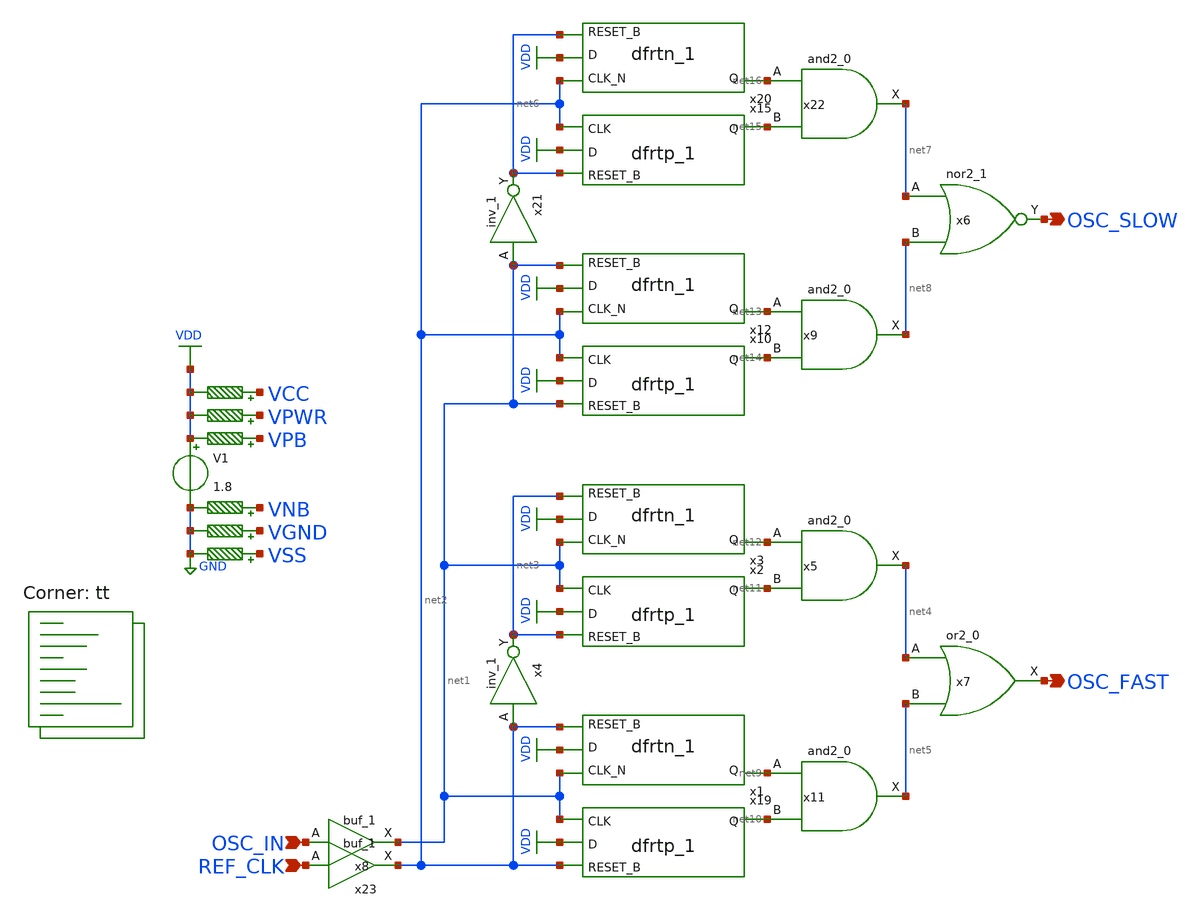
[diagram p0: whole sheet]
** sch_path: freq_det.sch
**.subckt freq_det OSC_IN REF_CLK OSC_FAST OSC_SLOW
*.ipin OSC_IN
*.ipin REF_CLK
*.opin OSC_FAST
*.opin OSC_SLOW
x8 OSC_IN VGND VNB VPB VPWR net1 sky130_fd_sc_hd__buf_1
x7 net4 net5 VGND VNB VPB VPWR OSC_FAST sky130_fd_sc_hd__or2_0
x11 net9 net10 VGND VNB VPB VPWR net5 sky130_fd_sc_hd__and2_0
x19 net1 VDD net2 VGND VNB VPB VPWR net10 sky130_fd_sc_hd__dfrtp_1
x1 net1 VDD net2 VGND VNB VPB VPWR net9 sky130_fd_sc_hd__dfrtn_1
x2 net1 VDD net3 VGND VNB VPB VPWR net11 sky130_fd_sc_hd__dfrtp_1
x3 net1 VDD net3 VGND VNB VPB VPWR net12 sky130_fd_sc_hd__dfrtn_1
x4 net2 VGND VNB VPB VPWR net3 sky130_fd_sc_hd__inv_1
x5 net12 net11 VGND VNB VPB VPWR net4 sky130_fd_sc_hd__and2_0
x9 net13 net14 VGND VNB VPB VPWR net8 sky130_fd_sc_hd__and2_0
x10 net2 VDD net1 VGND VNB VPB VPWR net14 sky130_fd_sc_hd__dfrtp_1
x12 net2 VDD net1 VGND VNB VPB VPWR net13 sky130_fd_sc_hd__dfrtn_1
x15 net2 VDD net6 VGND VNB VPB VPWR net15 sky130_fd_sc_hd__dfrtp_1
x20 net2 VDD net6 VGND VNB VPB VPWR net16 sky130_fd_sc_hd__dfrtn_1
x21 net1 VGND VNB VPB VPWR net6 sky130_fd_sc_hd__inv_1
x22 net16 net15 VGND VNB VPB VPWR net7 sky130_fd_sc_hd__and2_0
x6 net7 net8 VGND VNB VPB VPWR OSC_SLOW sky130_fd_sc_hd__nor2_1
x23 REF_CLK VGND VNB VPB VPWR net2 sky130_fd_sc_hd__buf_1
V1 VDD GND 1.8
R1 VPB VDD 0.01 m=1
R2 VPWR VDD 0.01 m=1
R3 VCC VDD 0.01 m=1
R4 VNB GND 0.01 m=1
R5 VGND GND 0.01 m=1
R6 VSS GND 0.01 m=1
**** begin user architecture code
.lib $::SKYWATER_MODELS/sky130.lib.spice tt


.include /usr/local/share/pdk/sky130A/libs.ref/sky130_fd_sc_hd/spice/sky130_fd_sc_hd.spice tt
.control
  save all
  tran 1n 10u
  write top.raw
  quit 0
.endc


**** end user architecture code
**.ends
.GLOBAL VDD
.GLOBAL GND
**** begin user architecture code


.GLOBAL VDD
.GLOBAL GND
.GLOBAL VCC
.GLOBAL VPWR
.GLOBAL VPB
.GLOBAL VNB
.GLOBAL VGND
.GLOBAL VSS


**** end user architecture code
.end
